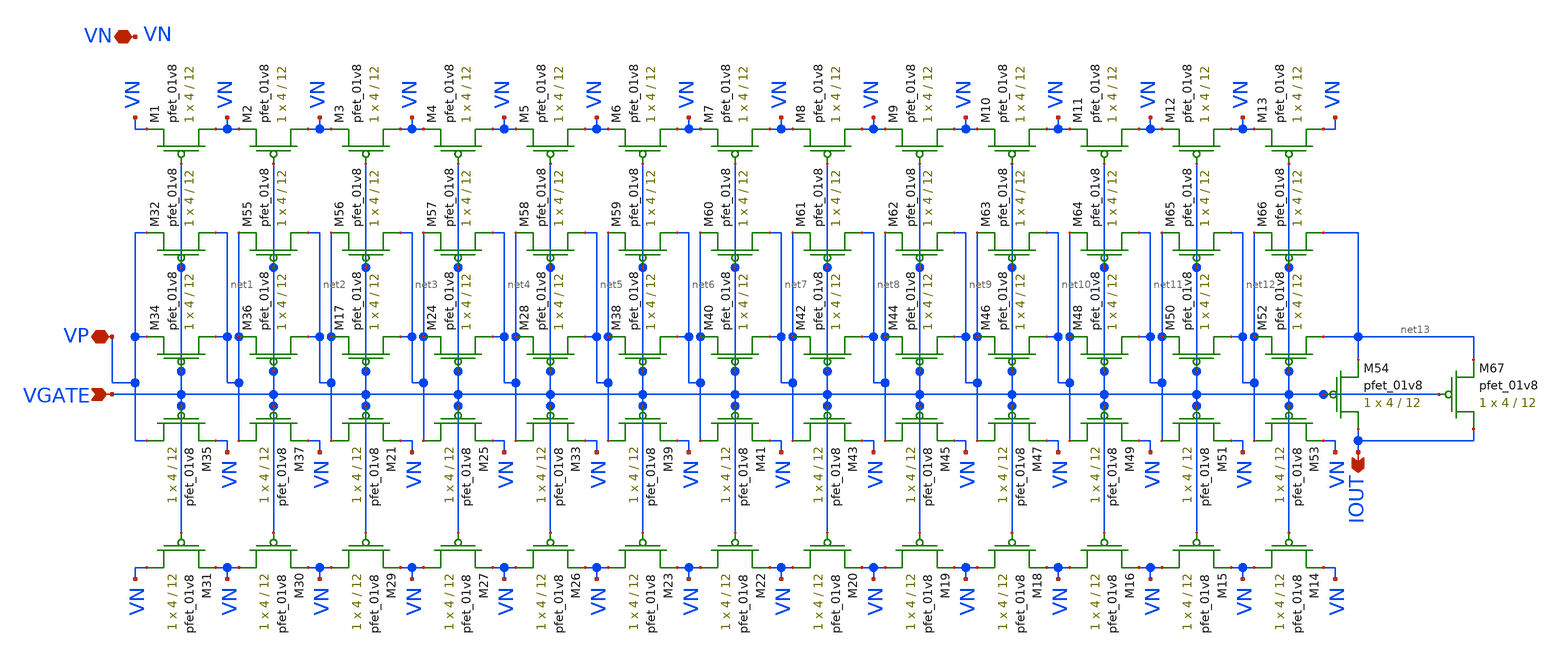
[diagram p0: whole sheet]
** sch_path: lib/analog/schematic/current_divider_layout_backup.sch
**.subckt current_divider_layout_backup VN IOUT VGATE VP
*.iopin VN
*.opin IOUT
*.ipin VGATE
*.iopin VP
XM34 net1 VGATE VP VDD sky130_fd_pr__pfet_01v8 L=12 W=4 nf=1 ad='int((nf+1)/2) * W/nf * 0.29' as='int((nf+2)/2) * W/nf * 0.29'
+ pd='2*int((nf+1)/2) * (W/nf + 0.29)' ps='2*int((nf+2)/2) * (W/nf + 0.29)' nrd='0.29 / W' nrs='0.29 / W'
+ sa=0 sb=0 sd=0 mult=1 m=1
XM35 VP VGATE VN VDD sky130_fd_pr__pfet_01v8 L=12 W=4 nf=1 ad='int((nf+1)/2) * W/nf * 0.29' as='int((nf+2)/2) * W/nf * 0.29'
+ pd='2*int((nf+1)/2) * (W/nf + 0.29)' ps='2*int((nf+2)/2) * (W/nf + 0.29)' nrd='0.29 / W' nrs='0.29 / W'
+ sa=0 sb=0 sd=0 mult=1 m=1
XM36 net2 VGATE net1 VDD sky130_fd_pr__pfet_01v8 L=12 W=4 nf=1 ad='int((nf+1)/2) * W/nf * 0.29' as='int((nf+2)/2) * W/nf * 0.29'
+ pd='2*int((nf+1)/2) * (W/nf + 0.29)' ps='2*int((nf+2)/2) * (W/nf + 0.29)' nrd='0.29 / W' nrs='0.29 / W'
+ sa=0 sb=0 sd=0 mult=1 m=1
XM37 net1 VGATE VN VDD sky130_fd_pr__pfet_01v8 L=12 W=4 nf=1 ad='int((nf+1)/2) * W/nf * 0.29' as='int((nf+2)/2) * W/nf * 0.29'
+ pd='2*int((nf+1)/2) * (W/nf + 0.29)' ps='2*int((nf+2)/2) * (W/nf + 0.29)' nrd='0.29 / W' nrs='0.29 / W'
+ sa=0 sb=0 sd=0 mult=1 m=1
XM17 net3 VGATE net2 VDD sky130_fd_pr__pfet_01v8 L=12 W=4 nf=1 ad='int((nf+1)/2) * W/nf * 0.29' as='int((nf+2)/2) * W/nf * 0.29'
+ pd='2*int((nf+1)/2) * (W/nf + 0.29)' ps='2*int((nf+2)/2) * (W/nf + 0.29)' nrd='0.29 / W' nrs='0.29 / W'
+ sa=0 sb=0 sd=0 mult=1 m=1
XM21 net2 VGATE VN VDD sky130_fd_pr__pfet_01v8 L=12 W=4 nf=1 ad='int((nf+1)/2) * W/nf * 0.29' as='int((nf+2)/2) * W/nf * 0.29'
+ pd='2*int((nf+1)/2) * (W/nf + 0.29)' ps='2*int((nf+2)/2) * (W/nf + 0.29)' nrd='0.29 / W' nrs='0.29 / W'
+ sa=0 sb=0 sd=0 mult=1 m=1
XM24 net4 VGATE net3 VDD sky130_fd_pr__pfet_01v8 L=12 W=4 nf=1 ad='int((nf+1)/2) * W/nf * 0.29' as='int((nf+2)/2) * W/nf * 0.29'
+ pd='2*int((nf+1)/2) * (W/nf + 0.29)' ps='2*int((nf+2)/2) * (W/nf + 0.29)' nrd='0.29 / W' nrs='0.29 / W'
+ sa=0 sb=0 sd=0 mult=1 m=1
XM25 net3 VGATE VN VDD sky130_fd_pr__pfet_01v8 L=12 W=4 nf=1 ad='int((nf+1)/2) * W/nf * 0.29' as='int((nf+2)/2) * W/nf * 0.29'
+ pd='2*int((nf+1)/2) * (W/nf + 0.29)' ps='2*int((nf+2)/2) * (W/nf + 0.29)' nrd='0.29 / W' nrs='0.29 / W'
+ sa=0 sb=0 sd=0 mult=1 m=1
XM28 net5 VGATE net4 VDD sky130_fd_pr__pfet_01v8 L=12 W=4 nf=1 ad='int((nf+1)/2) * W/nf * 0.29' as='int((nf+2)/2) * W/nf * 0.29'
+ pd='2*int((nf+1)/2) * (W/nf + 0.29)' ps='2*int((nf+2)/2) * (W/nf + 0.29)' nrd='0.29 / W' nrs='0.29 / W'
+ sa=0 sb=0 sd=0 mult=1 m=1
XM33 net4 VGATE VN VDD sky130_fd_pr__pfet_01v8 L=12 W=4 nf=1 ad='int((nf+1)/2) * W/nf * 0.29' as='int((nf+2)/2) * W/nf * 0.29'
+ pd='2*int((nf+1)/2) * (W/nf + 0.29)' ps='2*int((nf+2)/2) * (W/nf + 0.29)' nrd='0.29 / W' nrs='0.29 / W'
+ sa=0 sb=0 sd=0 mult=1 m=1
XM38 net6 VGATE net5 VDD sky130_fd_pr__pfet_01v8 L=12 W=4 nf=1 ad='int((nf+1)/2) * W/nf * 0.29' as='int((nf+2)/2) * W/nf * 0.29'
+ pd='2*int((nf+1)/2) * (W/nf + 0.29)' ps='2*int((nf+2)/2) * (W/nf + 0.29)' nrd='0.29 / W' nrs='0.29 / W'
+ sa=0 sb=0 sd=0 mult=1 m=1
XM39 net5 VGATE VN VDD sky130_fd_pr__pfet_01v8 L=12 W=4 nf=1 ad='int((nf+1)/2) * W/nf * 0.29' as='int((nf+2)/2) * W/nf * 0.29'
+ pd='2*int((nf+1)/2) * (W/nf + 0.29)' ps='2*int((nf+2)/2) * (W/nf + 0.29)' nrd='0.29 / W' nrs='0.29 / W'
+ sa=0 sb=0 sd=0 mult=1 m=1
XM40 net7 VGATE net6 VDD sky130_fd_pr__pfet_01v8 L=12 W=4 nf=1 ad='int((nf+1)/2) * W/nf * 0.29' as='int((nf+2)/2) * W/nf * 0.29'
+ pd='2*int((nf+1)/2) * (W/nf + 0.29)' ps='2*int((nf+2)/2) * (W/nf + 0.29)' nrd='0.29 / W' nrs='0.29 / W'
+ sa=0 sb=0 sd=0 mult=1 m=1
XM41 net6 VGATE VN VDD sky130_fd_pr__pfet_01v8 L=12 W=4 nf=1 ad='int((nf+1)/2) * W/nf * 0.29' as='int((nf+2)/2) * W/nf * 0.29'
+ pd='2*int((nf+1)/2) * (W/nf + 0.29)' ps='2*int((nf+2)/2) * (W/nf + 0.29)' nrd='0.29 / W' nrs='0.29 / W'
+ sa=0 sb=0 sd=0 mult=1 m=1
XM42 net8 VGATE net7 VDD sky130_fd_pr__pfet_01v8 L=12 W=4 nf=1 ad='int((nf+1)/2) * W/nf * 0.29' as='int((nf+2)/2) * W/nf * 0.29'
+ pd='2*int((nf+1)/2) * (W/nf + 0.29)' ps='2*int((nf+2)/2) * (W/nf + 0.29)' nrd='0.29 / W' nrs='0.29 / W'
+ sa=0 sb=0 sd=0 mult=1 m=1
XM43 net7 VGATE VN VDD sky130_fd_pr__pfet_01v8 L=12 W=4 nf=1 ad='int((nf+1)/2) * W/nf * 0.29' as='int((nf+2)/2) * W/nf * 0.29'
+ pd='2*int((nf+1)/2) * (W/nf + 0.29)' ps='2*int((nf+2)/2) * (W/nf + 0.29)' nrd='0.29 / W' nrs='0.29 / W'
+ sa=0 sb=0 sd=0 mult=1 m=1
XM44 net9 VGATE net8 VDD sky130_fd_pr__pfet_01v8 L=12 W=4 nf=1 ad='int((nf+1)/2) * W/nf * 0.29' as='int((nf+2)/2) * W/nf * 0.29'
+ pd='2*int((nf+1)/2) * (W/nf + 0.29)' ps='2*int((nf+2)/2) * (W/nf + 0.29)' nrd='0.29 / W' nrs='0.29 / W'
+ sa=0 sb=0 sd=0 mult=1 m=1
XM45 net8 VGATE VN VDD sky130_fd_pr__pfet_01v8 L=12 W=4 nf=1 ad='int((nf+1)/2) * W/nf * 0.29' as='int((nf+2)/2) * W/nf * 0.29'
+ pd='2*int((nf+1)/2) * (W/nf + 0.29)' ps='2*int((nf+2)/2) * (W/nf + 0.29)' nrd='0.29 / W' nrs='0.29 / W'
+ sa=0 sb=0 sd=0 mult=1 m=1
XM46 net10 VGATE net9 VDD sky130_fd_pr__pfet_01v8 L=12 W=4 nf=1 ad='int((nf+1)/2) * W/nf * 0.29' as='int((nf+2)/2) * W/nf * 0.29'
+ pd='2*int((nf+1)/2) * (W/nf + 0.29)' ps='2*int((nf+2)/2) * (W/nf + 0.29)' nrd='0.29 / W' nrs='0.29 / W'
+ sa=0 sb=0 sd=0 mult=1 m=1
XM47 net9 VGATE VN VDD sky130_fd_pr__pfet_01v8 L=12 W=4 nf=1 ad='int((nf+1)/2) * W/nf * 0.29' as='int((nf+2)/2) * W/nf * 0.29'
+ pd='2*int((nf+1)/2) * (W/nf + 0.29)' ps='2*int((nf+2)/2) * (W/nf + 0.29)' nrd='0.29 / W' nrs='0.29 / W'
+ sa=0 sb=0 sd=0 mult=1 m=1
XM48 net11 VGATE net10 VDD sky130_fd_pr__pfet_01v8 L=12 W=4 nf=1 ad='int((nf+1)/2) * W/nf * 0.29' as='int((nf+2)/2) * W/nf * 0.29'
+ pd='2*int((nf+1)/2) * (W/nf + 0.29)' ps='2*int((nf+2)/2) * (W/nf + 0.29)' nrd='0.29 / W' nrs='0.29 / W'
+ sa=0 sb=0 sd=0 mult=1 m=1
XM49 net10 VGATE VN VDD sky130_fd_pr__pfet_01v8 L=12 W=4 nf=1 ad='int((nf+1)/2) * W/nf * 0.29' as='int((nf+2)/2) * W/nf * 0.29'
+ pd='2*int((nf+1)/2) * (W/nf + 0.29)' ps='2*int((nf+2)/2) * (W/nf + 0.29)' nrd='0.29 / W' nrs='0.29 / W'
+ sa=0 sb=0 sd=0 mult=1 m=1
XM50 net12 VGATE net11 VDD sky130_fd_pr__pfet_01v8 L=12 W=4 nf=1 ad='int((nf+1)/2) * W/nf * 0.29' as='int((nf+2)/2) * W/nf * 0.29'
+ pd='2*int((nf+1)/2) * (W/nf + 0.29)' ps='2*int((nf+2)/2) * (W/nf + 0.29)' nrd='0.29 / W' nrs='0.29 / W'
+ sa=0 sb=0 sd=0 mult=1 m=1
XM51 net11 VGATE VN VDD sky130_fd_pr__pfet_01v8 L=12 W=4 nf=1 ad='int((nf+1)/2) * W/nf * 0.29' as='int((nf+2)/2) * W/nf * 0.29'
+ pd='2*int((nf+1)/2) * (W/nf + 0.29)' ps='2*int((nf+2)/2) * (W/nf + 0.29)' nrd='0.29 / W' nrs='0.29 / W'
+ sa=0 sb=0 sd=0 mult=1 m=1
XM52 net13 VGATE net12 VDD sky130_fd_pr__pfet_01v8 L=12 W=4 nf=1 ad='int((nf+1)/2) * W/nf * 0.29' as='int((nf+2)/2) * W/nf * 0.29'
+ pd='2*int((nf+1)/2) * (W/nf + 0.29)' ps='2*int((nf+2)/2) * (W/nf + 0.29)' nrd='0.29 / W' nrs='0.29 / W'
+ sa=0 sb=0 sd=0 mult=1 m=1
XM53 net12 VGATE VN VDD sky130_fd_pr__pfet_01v8 L=12 W=4 nf=1 ad='int((nf+1)/2) * W/nf * 0.29' as='int((nf+2)/2) * W/nf * 0.29'
+ pd='2*int((nf+1)/2) * (W/nf + 0.29)' ps='2*int((nf+2)/2) * (W/nf + 0.29)' nrd='0.29 / W' nrs='0.29 / W'
+ sa=0 sb=0 sd=0 mult=1 m=1
XM54 IOUT VGATE net13 VDD sky130_fd_pr__pfet_01v8 L=12 W=4 nf=1 ad='int((nf+1)/2) * W/nf * 0.29' as='int((nf+2)/2) * W/nf * 0.29'
+ pd='2*int((nf+1)/2) * (W/nf + 0.29)' ps='2*int((nf+2)/2) * (W/nf + 0.29)' nrd='0.29 / W' nrs='0.29 / W'
+ sa=0 sb=0 sd=0 mult=1 m=1
XM1 VN VGATE VN VDD sky130_fd_pr__pfet_01v8 L=12 W=4 nf=1 ad='int((nf+1)/2) * W/nf * 0.29' as='int((nf+2)/2) * W/nf * 0.29'
+ pd='2*int((nf+1)/2) * (W/nf + 0.29)' ps='2*int((nf+2)/2) * (W/nf + 0.29)' nrd='0.29 / W' nrs='0.29 / W'
+ sa=0 sb=0 sd=0 mult=1 m=1
XM2 VN VGATE VN VDD sky130_fd_pr__pfet_01v8 L=12 W=4 nf=1 ad='int((nf+1)/2) * W/nf * 0.29' as='int((nf+2)/2) * W/nf * 0.29'
+ pd='2*int((nf+1)/2) * (W/nf + 0.29)' ps='2*int((nf+2)/2) * (W/nf + 0.29)' nrd='0.29 / W' nrs='0.29 / W'
+ sa=0 sb=0 sd=0 mult=1 m=1
XM3 VN VGATE VN VDD sky130_fd_pr__pfet_01v8 L=12 W=4 nf=1 ad='int((nf+1)/2) * W/nf * 0.29' as='int((nf+2)/2) * W/nf * 0.29'
+ pd='2*int((nf+1)/2) * (W/nf + 0.29)' ps='2*int((nf+2)/2) * (W/nf + 0.29)' nrd='0.29 / W' nrs='0.29 / W'
+ sa=0 sb=0 sd=0 mult=1 m=1
XM4 VN VGATE VN VDD sky130_fd_pr__pfet_01v8 L=12 W=4 nf=1 ad='int((nf+1)/2) * W/nf * 0.29' as='int((nf+2)/2) * W/nf * 0.29'
+ pd='2*int((nf+1)/2) * (W/nf + 0.29)' ps='2*int((nf+2)/2) * (W/nf + 0.29)' nrd='0.29 / W' nrs='0.29 / W'
+ sa=0 sb=0 sd=0 mult=1 m=1
XM5 VN VGATE VN VDD sky130_fd_pr__pfet_01v8 L=12 W=4 nf=1 ad='int((nf+1)/2) * W/nf * 0.29' as='int((nf+2)/2) * W/nf * 0.29'
+ pd='2*int((nf+1)/2) * (W/nf + 0.29)' ps='2*int((nf+2)/2) * (W/nf + 0.29)' nrd='0.29 / W' nrs='0.29 / W'
+ sa=0 sb=0 sd=0 mult=1 m=1
XM6 VN VGATE VN VDD sky130_fd_pr__pfet_01v8 L=12 W=4 nf=1 ad='int((nf+1)/2) * W/nf * 0.29' as='int((nf+2)/2) * W/nf * 0.29'
+ pd='2*int((nf+1)/2) * (W/nf + 0.29)' ps='2*int((nf+2)/2) * (W/nf + 0.29)' nrd='0.29 / W' nrs='0.29 / W'
+ sa=0 sb=0 sd=0 mult=1 m=1
XM7 VN VGATE VN VDD sky130_fd_pr__pfet_01v8 L=12 W=4 nf=1 ad='int((nf+1)/2) * W/nf * 0.29' as='int((nf+2)/2) * W/nf * 0.29'
+ pd='2*int((nf+1)/2) * (W/nf + 0.29)' ps='2*int((nf+2)/2) * (W/nf + 0.29)' nrd='0.29 / W' nrs='0.29 / W'
+ sa=0 sb=0 sd=0 mult=1 m=1
XM8 VN VGATE VN VDD sky130_fd_pr__pfet_01v8 L=12 W=4 nf=1 ad='int((nf+1)/2) * W/nf * 0.29' as='int((nf+2)/2) * W/nf * 0.29'
+ pd='2*int((nf+1)/2) * (W/nf + 0.29)' ps='2*int((nf+2)/2) * (W/nf + 0.29)' nrd='0.29 / W' nrs='0.29 / W'
+ sa=0 sb=0 sd=0 mult=1 m=1
XM9 VN VGATE VN VDD sky130_fd_pr__pfet_01v8 L=12 W=4 nf=1 ad='int((nf+1)/2) * W/nf * 0.29' as='int((nf+2)/2) * W/nf * 0.29'
+ pd='2*int((nf+1)/2) * (W/nf + 0.29)' ps='2*int((nf+2)/2) * (W/nf + 0.29)' nrd='0.29 / W' nrs='0.29 / W'
+ sa=0 sb=0 sd=0 mult=1 m=1
XM10 VN VGATE VN VDD sky130_fd_pr__pfet_01v8 L=12 W=4 nf=1 ad='int((nf+1)/2) * W/nf * 0.29' as='int((nf+2)/2) * W/nf * 0.29'
+ pd='2*int((nf+1)/2) * (W/nf + 0.29)' ps='2*int((nf+2)/2) * (W/nf + 0.29)' nrd='0.29 / W' nrs='0.29 / W'
+ sa=0 sb=0 sd=0 mult=1 m=1
XM11 VN VGATE VN VDD sky130_fd_pr__pfet_01v8 L=12 W=4 nf=1 ad='int((nf+1)/2) * W/nf * 0.29' as='int((nf+2)/2) * W/nf * 0.29'
+ pd='2*int((nf+1)/2) * (W/nf + 0.29)' ps='2*int((nf+2)/2) * (W/nf + 0.29)' nrd='0.29 / W' nrs='0.29 / W'
+ sa=0 sb=0 sd=0 mult=1 m=1
XM12 VN VGATE VN VDD sky130_fd_pr__pfet_01v8 L=12 W=4 nf=1 ad='int((nf+1)/2) * W/nf * 0.29' as='int((nf+2)/2) * W/nf * 0.29'
+ pd='2*int((nf+1)/2) * (W/nf + 0.29)' ps='2*int((nf+2)/2) * (W/nf + 0.29)' nrd='0.29 / W' nrs='0.29 / W'
+ sa=0 sb=0 sd=0 mult=1 m=1
XM13 VN VGATE VN VDD sky130_fd_pr__pfet_01v8 L=12 W=4 nf=1 ad='int((nf+1)/2) * W/nf * 0.29' as='int((nf+2)/2) * W/nf * 0.29'
+ pd='2*int((nf+1)/2) * (W/nf + 0.29)' ps='2*int((nf+2)/2) * (W/nf + 0.29)' nrd='0.29 / W' nrs='0.29 / W'
+ sa=0 sb=0 sd=0 mult=1 m=1
XM14 VN VGATE VN VDD sky130_fd_pr__pfet_01v8 L=12 W=4 nf=1 ad='int((nf+1)/2) * W/nf * 0.29' as='int((nf+2)/2) * W/nf * 0.29'
+ pd='2*int((nf+1)/2) * (W/nf + 0.29)' ps='2*int((nf+2)/2) * (W/nf + 0.29)' nrd='0.29 / W' nrs='0.29 / W'
+ sa=0 sb=0 sd=0 mult=1 m=1
XM15 VN VGATE VN VDD sky130_fd_pr__pfet_01v8 L=12 W=4 nf=1 ad='int((nf+1)/2) * W/nf * 0.29' as='int((nf+2)/2) * W/nf * 0.29'
+ pd='2*int((nf+1)/2) * (W/nf + 0.29)' ps='2*int((nf+2)/2) * (W/nf + 0.29)' nrd='0.29 / W' nrs='0.29 / W'
+ sa=0 sb=0 sd=0 mult=1 m=1
XM16 VN VGATE VN VDD sky130_fd_pr__pfet_01v8 L=12 W=4 nf=1 ad='int((nf+1)/2) * W/nf * 0.29' as='int((nf+2)/2) * W/nf * 0.29'
+ pd='2*int((nf+1)/2) * (W/nf + 0.29)' ps='2*int((nf+2)/2) * (W/nf + 0.29)' nrd='0.29 / W' nrs='0.29 / W'
+ sa=0 sb=0 sd=0 mult=1 m=1
XM18 VN VGATE VN VDD sky130_fd_pr__pfet_01v8 L=12 W=4 nf=1 ad='int((nf+1)/2) * W/nf * 0.29' as='int((nf+2)/2) * W/nf * 0.29'
+ pd='2*int((nf+1)/2) * (W/nf + 0.29)' ps='2*int((nf+2)/2) * (W/nf + 0.29)' nrd='0.29 / W' nrs='0.29 / W'
+ sa=0 sb=0 sd=0 mult=1 m=1
XM19 VN VGATE VN VDD sky130_fd_pr__pfet_01v8 L=12 W=4 nf=1 ad='int((nf+1)/2) * W/nf * 0.29' as='int((nf+2)/2) * W/nf * 0.29'
+ pd='2*int((nf+1)/2) * (W/nf + 0.29)' ps='2*int((nf+2)/2) * (W/nf + 0.29)' nrd='0.29 / W' nrs='0.29 / W'
+ sa=0 sb=0 sd=0 mult=1 m=1
XM20 VN VGATE VN VDD sky130_fd_pr__pfet_01v8 L=12 W=4 nf=1 ad='int((nf+1)/2) * W/nf * 0.29' as='int((nf+2)/2) * W/nf * 0.29'
+ pd='2*int((nf+1)/2) * (W/nf + 0.29)' ps='2*int((nf+2)/2) * (W/nf + 0.29)' nrd='0.29 / W' nrs='0.29 / W'
+ sa=0 sb=0 sd=0 mult=1 m=1
XM22 VN VGATE VN VDD sky130_fd_pr__pfet_01v8 L=12 W=4 nf=1 ad='int((nf+1)/2) * W/nf * 0.29' as='int((nf+2)/2) * W/nf * 0.29'
+ pd='2*int((nf+1)/2) * (W/nf + 0.29)' ps='2*int((nf+2)/2) * (W/nf + 0.29)' nrd='0.29 / W' nrs='0.29 / W'
+ sa=0 sb=0 sd=0 mult=1 m=1
XM23 VN VGATE VN VDD sky130_fd_pr__pfet_01v8 L=12 W=4 nf=1 ad='int((nf+1)/2) * W/nf * 0.29' as='int((nf+2)/2) * W/nf * 0.29'
+ pd='2*int((nf+1)/2) * (W/nf + 0.29)' ps='2*int((nf+2)/2) * (W/nf + 0.29)' nrd='0.29 / W' nrs='0.29 / W'
+ sa=0 sb=0 sd=0 mult=1 m=1
XM26 VN VGATE VN VDD sky130_fd_pr__pfet_01v8 L=12 W=4 nf=1 ad='int((nf+1)/2) * W/nf * 0.29' as='int((nf+2)/2) * W/nf * 0.29'
+ pd='2*int((nf+1)/2) * (W/nf + 0.29)' ps='2*int((nf+2)/2) * (W/nf + 0.29)' nrd='0.29 / W' nrs='0.29 / W'
+ sa=0 sb=0 sd=0 mult=1 m=1
XM27 VN VGATE VN VDD sky130_fd_pr__pfet_01v8 L=12 W=4 nf=1 ad='int((nf+1)/2) * W/nf * 0.29' as='int((nf+2)/2) * W/nf * 0.29'
+ pd='2*int((nf+1)/2) * (W/nf + 0.29)' ps='2*int((nf+2)/2) * (W/nf + 0.29)' nrd='0.29 / W' nrs='0.29 / W'
+ sa=0 sb=0 sd=0 mult=1 m=1
XM29 VN VGATE VN VDD sky130_fd_pr__pfet_01v8 L=12 W=4 nf=1 ad='int((nf+1)/2) * W/nf * 0.29' as='int((nf+2)/2) * W/nf * 0.29'
+ pd='2*int((nf+1)/2) * (W/nf + 0.29)' ps='2*int((nf+2)/2) * (W/nf + 0.29)' nrd='0.29 / W' nrs='0.29 / W'
+ sa=0 sb=0 sd=0 mult=1 m=1
XM30 VN VGATE VN VDD sky130_fd_pr__pfet_01v8 L=12 W=4 nf=1 ad='int((nf+1)/2) * W/nf * 0.29' as='int((nf+2)/2) * W/nf * 0.29'
+ pd='2*int((nf+1)/2) * (W/nf + 0.29)' ps='2*int((nf+2)/2) * (W/nf + 0.29)' nrd='0.29 / W' nrs='0.29 / W'
+ sa=0 sb=0 sd=0 mult=1 m=1
XM31 VN VGATE VN VDD sky130_fd_pr__pfet_01v8 L=12 W=4 nf=1 ad='int((nf+1)/2) * W/nf * 0.29' as='int((nf+2)/2) * W/nf * 0.29'
+ pd='2*int((nf+1)/2) * (W/nf + 0.29)' ps='2*int((nf+2)/2) * (W/nf + 0.29)' nrd='0.29 / W' nrs='0.29 / W'
+ sa=0 sb=0 sd=0 mult=1 m=1
XM32 net1 VGATE VP VDD sky130_fd_pr__pfet_01v8 L=12 W=4 nf=1 ad='int((nf+1)/2) * W/nf * 0.29' as='int((nf+2)/2) * W/nf * 0.29'
+ pd='2*int((nf+1)/2) * (W/nf + 0.29)' ps='2*int((nf+2)/2) * (W/nf + 0.29)' nrd='0.29 / W' nrs='0.29 / W'
+ sa=0 sb=0 sd=0 mult=1 m=1
XM55 net2 VGATE net1 VDD sky130_fd_pr__pfet_01v8 L=12 W=4 nf=1 ad='int((nf+1)/2) * W/nf * 0.29' as='int((nf+2)/2) * W/nf * 0.29'
+ pd='2*int((nf+1)/2) * (W/nf + 0.29)' ps='2*int((nf+2)/2) * (W/nf + 0.29)' nrd='0.29 / W' nrs='0.29 / W'
+ sa=0 sb=0 sd=0 mult=1 m=1
XM56 net3 VGATE net2 VDD sky130_fd_pr__pfet_01v8 L=12 W=4 nf=1 ad='int((nf+1)/2) * W/nf * 0.29' as='int((nf+2)/2) * W/nf * 0.29'
+ pd='2*int((nf+1)/2) * (W/nf + 0.29)' ps='2*int((nf+2)/2) * (W/nf + 0.29)' nrd='0.29 / W' nrs='0.29 / W'
+ sa=0 sb=0 sd=0 mult=1 m=1
XM57 net4 VGATE net3 VDD sky130_fd_pr__pfet_01v8 L=12 W=4 nf=1 ad='int((nf+1)/2) * W/nf * 0.29' as='int((nf+2)/2) * W/nf * 0.29'
+ pd='2*int((nf+1)/2) * (W/nf + 0.29)' ps='2*int((nf+2)/2) * (W/nf + 0.29)' nrd='0.29 / W' nrs='0.29 / W'
+ sa=0 sb=0 sd=0 mult=1 m=1
XM58 net5 VGATE net4 VDD sky130_fd_pr__pfet_01v8 L=12 W=4 nf=1 ad='int((nf+1)/2) * W/nf * 0.29' as='int((nf+2)/2) * W/nf * 0.29'
+ pd='2*int((nf+1)/2) * (W/nf + 0.29)' ps='2*int((nf+2)/2) * (W/nf + 0.29)' nrd='0.29 / W' nrs='0.29 / W'
+ sa=0 sb=0 sd=0 mult=1 m=1
XM59 net6 VGATE net5 VDD sky130_fd_pr__pfet_01v8 L=12 W=4 nf=1 ad='int((nf+1)/2) * W/nf * 0.29' as='int((nf+2)/2) * W/nf * 0.29'
+ pd='2*int((nf+1)/2) * (W/nf + 0.29)' ps='2*int((nf+2)/2) * (W/nf + 0.29)' nrd='0.29 / W' nrs='0.29 / W'
+ sa=0 sb=0 sd=0 mult=1 m=1
XM60 net7 VGATE net6 VDD sky130_fd_pr__pfet_01v8 L=12 W=4 nf=1 ad='int((nf+1)/2) * W/nf * 0.29' as='int((nf+2)/2) * W/nf * 0.29'
+ pd='2*int((nf+1)/2) * (W/nf + 0.29)' ps='2*int((nf+2)/2) * (W/nf + 0.29)' nrd='0.29 / W' nrs='0.29 / W'
+ sa=0 sb=0 sd=0 mult=1 m=1
XM61 net8 VGATE net7 VDD sky130_fd_pr__pfet_01v8 L=12 W=4 nf=1 ad='int((nf+1)/2) * W/nf * 0.29' as='int((nf+2)/2) * W/nf * 0.29'
+ pd='2*int((nf+1)/2) * (W/nf + 0.29)' ps='2*int((nf+2)/2) * (W/nf + 0.29)' nrd='0.29 / W' nrs='0.29 / W'
+ sa=0 sb=0 sd=0 mult=1 m=1
XM62 net9 VGATE net8 VDD sky130_fd_pr__pfet_01v8 L=12 W=4 nf=1 ad='int((nf+1)/2) * W/nf * 0.29' as='int((nf+2)/2) * W/nf * 0.29'
+ pd='2*int((nf+1)/2) * (W/nf + 0.29)' ps='2*int((nf+2)/2) * (W/nf + 0.29)' nrd='0.29 / W' nrs='0.29 / W'
+ sa=0 sb=0 sd=0 mult=1 m=1
XM63 net10 VGATE net9 VDD sky130_fd_pr__pfet_01v8 L=12 W=4 nf=1 ad='int((nf+1)/2) * W/nf * 0.29' as='int((nf+2)/2) * W/nf * 0.29'
+ pd='2*int((nf+1)/2) * (W/nf + 0.29)' ps='2*int((nf+2)/2) * (W/nf + 0.29)' nrd='0.29 / W' nrs='0.29 / W'
+ sa=0 sb=0 sd=0 mult=1 m=1
XM64 net11 VGATE net10 VDD sky130_fd_pr__pfet_01v8 L=12 W=4 nf=1 ad='int((nf+1)/2) * W/nf * 0.29' as='int((nf+2)/2) * W/nf * 0.29'
+ pd='2*int((nf+1)/2) * (W/nf + 0.29)' ps='2*int((nf+2)/2) * (W/nf + 0.29)' nrd='0.29 / W' nrs='0.29 / W'
+ sa=0 sb=0 sd=0 mult=1 m=1
XM65 net12 VGATE net11 VDD sky130_fd_pr__pfet_01v8 L=12 W=4 nf=1 ad='int((nf+1)/2) * W/nf * 0.29' as='int((nf+2)/2) * W/nf * 0.29'
+ pd='2*int((nf+1)/2) * (W/nf + 0.29)' ps='2*int((nf+2)/2) * (W/nf + 0.29)' nrd='0.29 / W' nrs='0.29 / W'
+ sa=0 sb=0 sd=0 mult=1 m=1
XM66 net13 VGATE net12 VDD sky130_fd_pr__pfet_01v8 L=12 W=4 nf=1 ad='int((nf+1)/2) * W/nf * 0.29' as='int((nf+2)/2) * W/nf * 0.29'
+ pd='2*int((nf+1)/2) * (W/nf + 0.29)' ps='2*int((nf+2)/2) * (W/nf + 0.29)' nrd='0.29 / W' nrs='0.29 / W'
+ sa=0 sb=0 sd=0 mult=1 m=1
XM67 IOUT VGATE net13 VDD sky130_fd_pr__pfet_01v8 L=12 W=4 nf=1 ad='int((nf+1)/2) * W/nf * 0.29' as='int((nf+2)/2) * W/nf * 0.29'
+ pd='2*int((nf+1)/2) * (W/nf + 0.29)' ps='2*int((nf+2)/2) * (W/nf + 0.29)' nrd='0.29 / W' nrs='0.29 / W'
+ sa=0 sb=0 sd=0 mult=1 m=1
**.ends
.end
